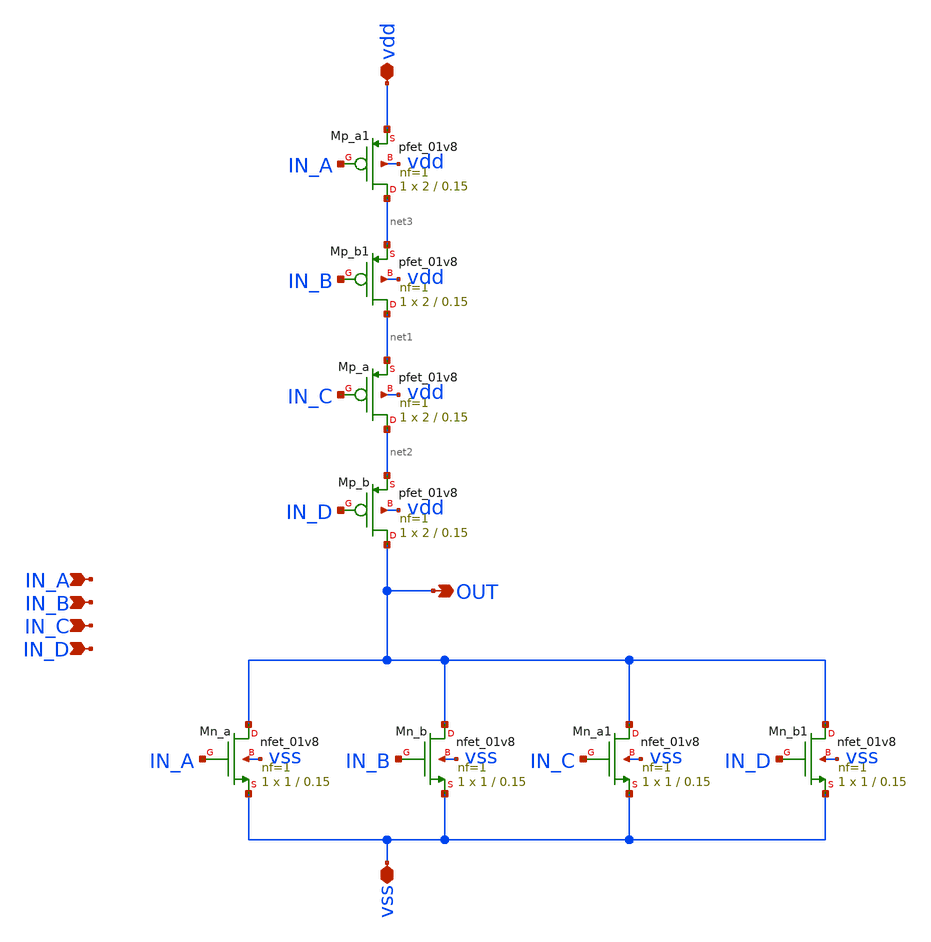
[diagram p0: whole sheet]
** sch_path: xsch/ip/logic/nor4/nor4.sch
**.subckt nor4 IN_A OUT vss vdd IN_B IN_C IN_D
*.ipin IN_A
*.opin OUT
*.iopin vss
*.iopin vdd
*.ipin IN_B
*.ipin IN_C
*.ipin IN_D
XMn_a OUT IN_A vss vss sky130_fd_pr__nfet_01v8 L=0.15 W=1 nf=1 ad='int((1 + 1)/2) * 1 / 1 * 0.29' as='int((1 + 2)/2) * 1 / 1 * 0.29'
+ pd='2*int((1 + 1)/2) * (1 / 1 + 0.29)' ps='2*int((1 + 2)/2) * (1 / 1 + 0.29)' nrd='0.29 / 1 ' nrs='0.29 / 1 '
+ sa=0 sb=0 sd=0 mult=1 m=1
XMp_a net2 IN_C net1 vdd sky130_fd_pr__pfet_01v8 L=0.15 W=2 nf=1 ad='int((nf+1)/2) * W/nf * 0.29' as='int((nf+2)/2) * W/nf * 0.29'
+ pd='2*int((nf+1)/2) * (W/nf + 0.29)' ps='2*int((nf+2)/2) * (W/nf + 0.29)' nrd='0.29 / W' nrs='0.29 / W'
+ sa=0 sb=0 sd=0 mult=1 m=1
XMp_b OUT IN_D net2 vdd sky130_fd_pr__pfet_01v8 L=0.15 W=2 nf=1 ad='int((nf+1)/2) * W/nf * 0.29' as='int((nf+2)/2) * W/nf * 0.29'
+ pd='2*int((nf+1)/2) * (W/nf + 0.29)' ps='2*int((nf+2)/2) * (W/nf + 0.29)' nrd='0.29 / W' nrs='0.29 / W'
+ sa=0 sb=0 sd=0 mult=1 m=1
XMn_b OUT IN_B vss vss sky130_fd_pr__nfet_01v8 L=0.15 W=1 nf=1 ad='int((1 + 1)/2) * 1 / 1 * 0.29' as='int((1 + 2)/2) * 1 / 1 * 0.29'
+ pd='2*int((1 + 1)/2) * (1 / 1 + 0.29)' ps='2*int((1 + 2)/2) * (1 / 1 + 0.29)' nrd='0.29 / 1 ' nrs='0.29 / 1 '
+ sa=0 sb=0 sd=0 mult=1 m=1
XMn_a1 OUT IN_C vss vss sky130_fd_pr__nfet_01v8 L=0.15 W=1 nf=1 ad='int((1 + 1)/2) * 1 / 1 * 0.29' as='int((1 + 2)/2) * 1 / 1 * 0.29'
+ pd='2*int((1 + 1)/2) * (1 / 1 + 0.29)' ps='2*int((1 + 2)/2) * (1 / 1 + 0.29)' nrd='0.29 / 1 ' nrs='0.29 / 1 '
+ sa=0 sb=0 sd=0 mult=1 m=1
XMn_b1 OUT IN_D vss vss sky130_fd_pr__nfet_01v8 L=0.15 W=1 nf=1 ad='int((1 + 1)/2) * 1 / 1 * 0.29' as='int((1 + 2)/2) * 1 / 1 * 0.29'
+ pd='2*int((1 + 1)/2) * (1 / 1 + 0.29)' ps='2*int((1 + 2)/2) * (1 / 1 + 0.29)' nrd='0.29 / 1 ' nrs='0.29 / 1 '
+ sa=0 sb=0 sd=0 mult=1 m=1
XMp_a1 net3 IN_A vdd vdd sky130_fd_pr__pfet_01v8 L=0.15 W=2 nf=1 ad='int((nf+1)/2) * W/nf * 0.29' as='int((nf+2)/2) * W/nf * 0.29'
+ pd='2*int((nf+1)/2) * (W/nf + 0.29)' ps='2*int((nf+2)/2) * (W/nf + 0.29)' nrd='0.29 / W' nrs='0.29 / W'
+ sa=0 sb=0 sd=0 mult=1 m=1
XMp_b1 net1 IN_B net3 vdd sky130_fd_pr__pfet_01v8 L=0.15 W=2 nf=1 ad='int((nf+1)/2) * W/nf * 0.29' as='int((nf+2)/2) * W/nf * 0.29'
+ pd='2*int((nf+1)/2) * (W/nf + 0.29)' ps='2*int((nf+2)/2) * (W/nf + 0.29)' nrd='0.29 / W' nrs='0.29 / W'
+ sa=0 sb=0 sd=0 mult=1 m=1
**.ends
.end
